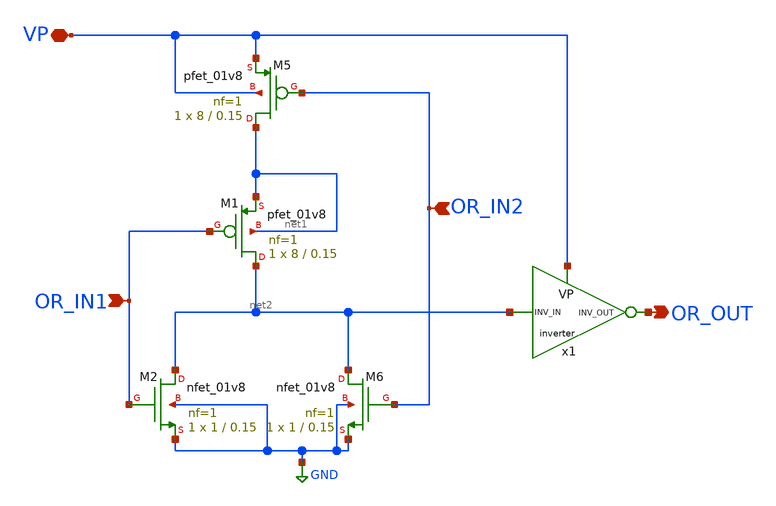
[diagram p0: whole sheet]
** sch_path: AllSymbols&Sch/Gates/StaticORGate.sch
**.subckt StaticORGate OR_IN1 OR_OUT OR_IN2 VP
*.ipin OR_IN1
*.opin OR_OUT
*.ipin OR_IN2
*.iopin VP
XM1 net2 OR_IN1 net1 net1 sky130_fd_pr__pfet_01v8 L=0.15 W=8 nf=1 ad='int((1 + 1)/2) * 8 / 1 * 0.29'
+ as='int((1 + 2)/2) * 8 / 1 * 0.29' pd='2*int((1 + 1)/2) * (8 / 1 + 0.29)' ps='2*int((1 + 2)/2) * (8 / 1 + 0.29)'
+ nrd='0.29 / 8 ' nrs='0.29 / 8 ' sa=0 sb=0 sd=0 mult=1 m=1
XM2 net2 OR_IN1 GND GND sky130_fd_pr__nfet_01v8 L=0.15 W=1 nf=1 ad='int((1 + 1)/2) * 1 / 1 * 0.29' as='int((1 + 2)/2) * 1 / 1 * 0.29'
+ pd='2*int((1 + 1)/2) * (1 / 1 + 0.29)' ps='2*int((1 + 2)/2) * (1 / 1 + 0.29)' nrd='0.29 / 1 ' nrs='0.29 / 1 '
+ sa=0 sb=0 sd=0 mult=1 m=1
XM5 net1 OR_IN2 VP VP sky130_fd_pr__pfet_01v8 L=0.15 W=8 nf=1 ad='int((1 + 1)/2) * 8 / 1 * 0.29' as='int((1 + 2)/2) * 8 / 1 * 0.29'
+ pd='2*int((1 + 1)/2) * (8 / 1 + 0.29)' ps='2*int((1 + 2)/2) * (8 / 1 + 0.29)' nrd='0.29 / 8 ' nrs='0.29 / 8 '
+ sa=0 sb=0 sd=0 mult=1 m=1
XM6 net2 OR_IN2 GND GND sky130_fd_pr__nfet_01v8 L=0.15 W=1 nf=1 ad='int((1 + 1)/2) * 1 / 1 * 0.29' as='int((1 + 2)/2) * 1 / 1 * 0.29'
+ pd='2*int((1 + 1)/2) * (1 / 1 + 0.29)' ps='2*int((1 + 2)/2) * (1 / 1 + 0.29)' nrd='0.29 / 1 ' nrs='0.29 / 1 '
+ sa=0 sb=0 sd=0 mult=1 m=1
x1 VP OR_OUT net2 inverter
**.ends

* expanding   symbol:
*+  /home/safal/projects/GitHub_CMOS_4bit_ALU/AllSymbols&Sch/GenericSym/inverter.sym # of pins=3
** sym_path: AllSymbols&Sch/GenericSym/inverter.sym
** sch_path: AllSymbols&Sch/GenericSym/inverter.sch
.subckt inverter VP inv_out inv_in
*.ipin inv_in
*.opin inv_out
*.iopin VP
XM1 inv_out inv_in VP VP sky130_fd_pr__pfet_01v8 L=0.15 W=2 nf=1 ad='int((1 + 1)/2) * 2 / 1 * 0.29' as='int((1 + 2)/2) * 2 / 1 * 0.29'
+ pd='2*int((1 + 1)/2) * (2 / 1 + 0.29)' ps='2*int((1 + 2)/2) * (2 / 1 + 0.29)' nrd='0.29 / 2 ' nrs='0.29 / 2 '
+ sa=0 sb=0 sd=0 mult=1 m=1
XM2 inv_out inv_in GND GND sky130_fd_pr__nfet_01v8 L=0.15 W=1 nf=1 ad='int((1 + 1)/2) * 1 / 1 * 0.29'
+ as='int((1 + 2)/2) * 1 / 1 * 0.29' pd='2*int((1 + 1)/2) * (1 / 1 + 0.29)' ps='2*int((1 + 2)/2) * (1 / 1 + 0.29)'
+ nrd='0.29 / 1 ' nrs='0.29 / 1 ' sa=0 sb=0 sd=0 mult=1 m=1
.ends

.GLOBAL GND
.end
